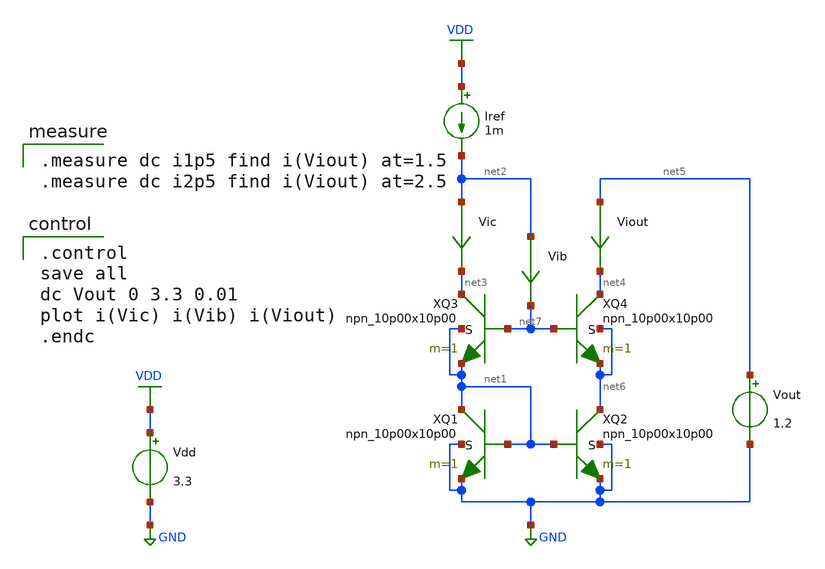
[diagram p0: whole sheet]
** sch_path: current-source/cm-cascode-bjt.sch
**.subckt cm-cascode-bjt
XQ2 net6 net1 GND GND npn_10p00x10p00 m=1
XQ1 net1 net1 GND GND npn_10p00x10p00 m=1
Viout net5 net4 0
.save i(viout)
Vdd VDD GND 3.3
Iref VDD net2 1m
Vic net2 net3 0
.save i(vic)
Vib net2 net7 0
.save i(vib)
Vout net5 GND 1.2
XQ3 net3 net7 net1 net1 npn_10p00x10p00 m=1
XQ4 net4 net7 net6 net6 npn_10p00x10p00 m=1
**** begin user architecture code

.include $::180MCU_MODELS/design.ngspice
.lib $::180MCU_MODELS/sm141064.ngspice typical
.lib $::180MCU_MODELS/sm141064.ngspice res_typical
.lib $::180MCU_MODELS/sm141064.ngspice moscap_typical
.lib $::180MCU_MODELS/sm141064.ngspice bjt_typical
* .lib $::180MCU_MODELS/sm141064.ngspice res_statistical


.control
save all
dc Vout 0 3.3 0.01
plot i(Vic) i(Vib) i(Viout)
.endc


.measure dc i1p5 find i(Viout) at=1.5
.measure dc i2p5 find i(Viout) at=2.5

**** end user architecture code
**.ends
.GLOBAL GND
.GLOBAL VDD
.end
